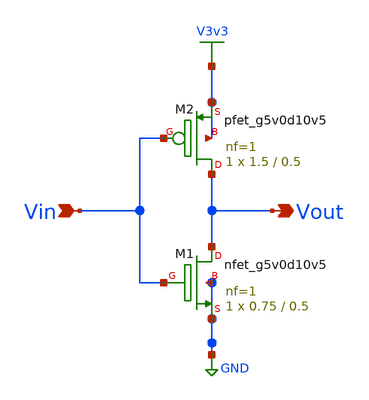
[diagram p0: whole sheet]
** sch_path: xschem/test/xschem/StandardCells/inverter.sch
**.subckt inverter Vout Vin
*.opin Vout
*.ipin Vin
XM1 Vout Vin GND GND sky130_fd_pr__nfet_g5v0d10v5 L=0.5 W=0.75 nf=1 ad='int((nf+1)/2) * W/nf * 0.29'
+ as='int((nf+2)/2) * W/nf * 0.29' pd='2*int((nf+1)/2) * (W/nf + 0.29)' ps='2*int((nf+2)/2) * (W/nf + 0.29)'
+ nrd='0.29 / W' nrs='0.29 / W' sa=0 sb=0 sd=0 mult=1 m=1
XM2 Vout Vin V3v3 V3v3 sky130_fd_pr__pfet_g5v0d10v5 L=0.5 W=1.5 nf=1 ad='int((nf+1)/2) * W/nf * 0.29'
+ as='int((nf+2)/2) * W/nf * 0.29' pd='2*int((nf+1)/2) * (W/nf + 0.29)' ps='2*int((nf+2)/2) * (W/nf + 0.29)'
+ nrd='0.29 / W' nrs='0.29 / W' sa=0 sb=0 sd=0 mult=1 m=1
**.ends
.GLOBAL V3v3
.GLOBAL GND
.end
